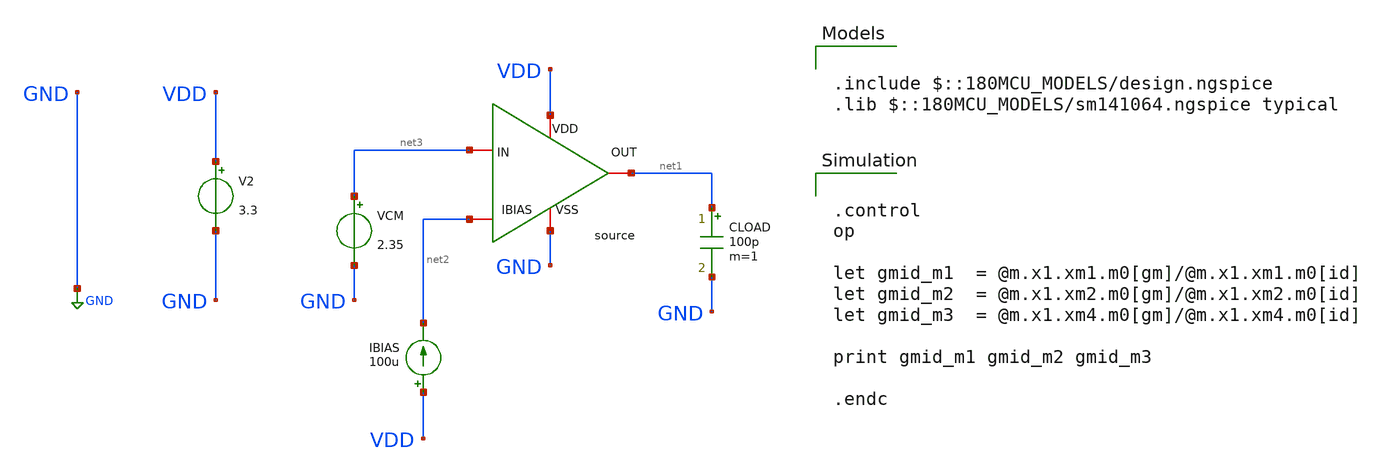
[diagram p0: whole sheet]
** sch_path: designs/libs/core_amps/cs_stage/op.sch
**.subckt op
x1 VDD net3 net2 net1 GND cs_schematic
V2 VDD GND 3.3
IBIAS VDD net2 100u
CLOAD net1 GND 100p m=1
VCM net3 GND 2.35
**** begin user architecture code

.include $::180MCU_MODELS/design.ngspice
.lib $::180MCU_MODELS/sm141064.ngspice typical



.control
op

let gmid_m1  = @m.x1.xm1.m0[gm]/@m.x1.xm1.m0[id]
let gmid_m2  = @m.x1.xm2.m0[gm]/@m.x1.xm2.m0[id]
let gmid_m3  = @m.x1.xm4.m0[gm]/@m.x1.xm4.m0[id]

print gmid_m1 gmid_m2 gmid_m3

.endc


**** end user architecture code
**.ends
.GLOBAL GND
.end
